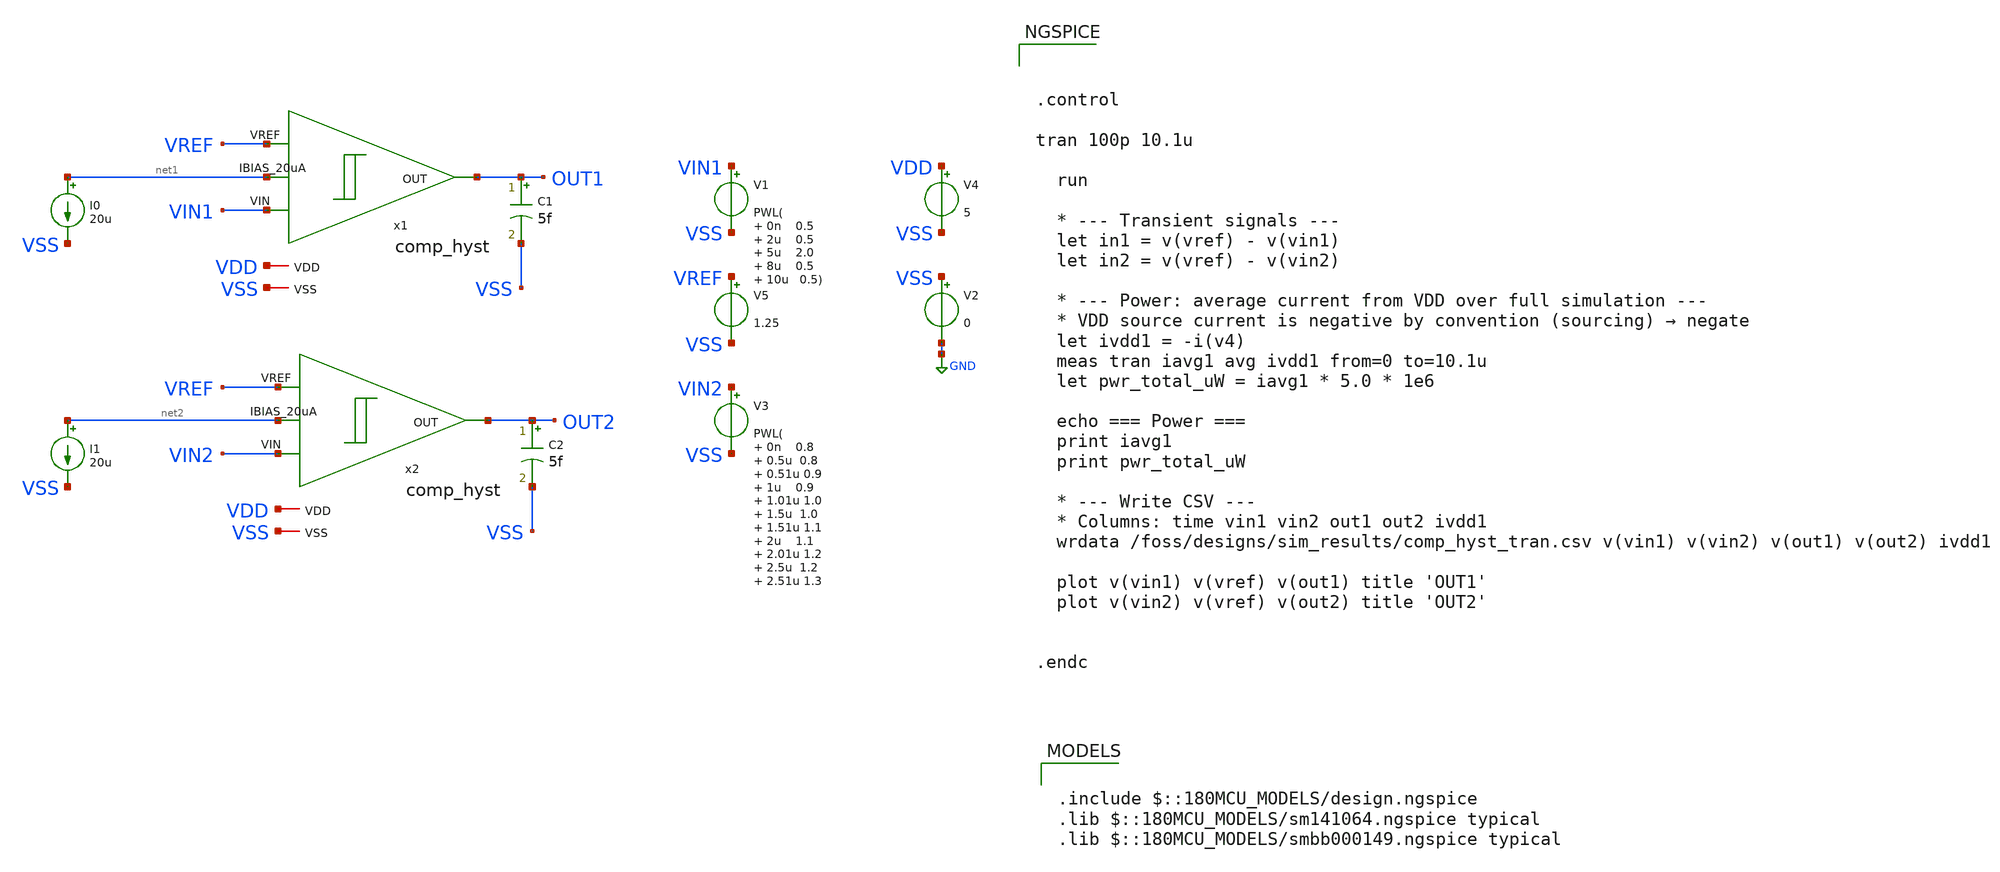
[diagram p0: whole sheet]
** sch_path: designs/hyst-comparator/tb_tran_comp_hyst.sch
**.subckt tb_tran_comp_hyst
I0 net1 VSS 20u
I1 net2 VSS 20u
C1 OUT1 VSS 5f m=1
C2 OUT2 VSS 5f m=1
V1 VIN1 VSS PWL( 0n 0.5 2u 0.5 5u 2.0 8u 0.5 10u 0.5)
V3 VIN2 VSS PWL( 0n 0.8 0.5u 0.8 0.51u 0.9 1u 0.9 1.01u 1.0 1.5u 1.0 1.51u 1.1 2u 1.1 2.01u 1.2 2.5u
+ 1.2 2.51u 1.3 3u 1.3 3.01u 1.4 3.5u 1.4 3.51u 1.5 4u 1.5 4.01u 1.6 4.5u 1.6 4.51u 1.5 5u 1.5 5.01u 1.4
+ 5.5u 1.4 5.51u 1.3 6u 1.3 6.01u 1.2 6.5u 1.2 6.51u 1.1 7u 1.1 7.01u 1.0 7.5u 1.0 7.51u 0.9 8u 0.9 8.01u
+ 0.8 10u 0.8)
V4 VDD VSS 5
V5 VREF VSS 1.25
V2 VSS GND 0
x1 VDD net1 VIN1 VREF OUT1 VSS comp_hyst
x2 VDD net2 VIN2 VREF OUT2 VSS comp_hyst
**** begin user architecture code



.control

tran 100p 10.1u

  run

  * --- Transient signals ---
  let in1 = v(vref) - v(vin1)
  let in2 = v(vref) - v(vin2)

  * --- Power: average current from VDD over full simulation ---
  * VDD source current is negative by convention (sourcing) → negate
  let ivdd1 = -i(v4)
  meas tran iavg1 avg ivdd1 from=0 to=10.1u
  let pwr_total_uW = iavg1 * 5.0 * 1e6

  echo === Power ===
  print iavg1
  print pwr_total_uW

  * --- Write CSV ---
  * Columns: time vin1 vin2 out1 out2 ivdd1
  wrdata /foss/designs/sim_results/comp_hyst_tran.csv v(vin1) v(vin2) v(out1) v(out2) ivdd1

  plot v(vin1) v(vref) v(out1) title 'OUT1'
  plot v(vin2) v(vref) v(out2) title 'OUT2'


.endc



.include $::180MCU_MODELS/design.ngspice
.lib $::180MCU_MODELS/sm141064.ngspice typical
.lib $::180MCU_MODELS/smbb000149.ngspice typical

**** end user architecture code
**.ends

* expanding   symbol:  comp_hyst.sym # of pins=6
** sym_path: designs/hyst-comparator/comp_hyst.sym
** sch_path: designs/hyst-comparator/comp_hyst.sch
.subckt comp_hyst VDD IBIAS_20uA VIN VREF OUT VSS
*.ipin VIN
*.ipin VREF
*.opin OUT
*.ipin IBIAS_20uA
*.iopin VDD
*.iopin VSS
XM1 net2 IBIAS_20uA VDD VDD pfet_05v0 L=1u W=11.8u nf=1 ad='int((nf+1)/2) * W/nf * 0.18u' as='int((nf+2)/2) * W/nf * 0.18u'
+ pd='2*int((nf+1)/2) * (W/nf + 0.18u)' ps='2*int((nf+2)/2) * (W/nf + 0.18u)' nrd='0.18u / W' nrs='0.18u / W'
+ sa=0 sb=0 sd=0 m=1
XM2 IBIAS_20uA IBIAS_20uA VDD VDD pfet_05v0 L=1u W=11.8u nf=1 ad='int((nf+1)/2) * W/nf * 0.18u' as='int((nf+2)/2) * W/nf * 0.18u'
+ pd='2*int((nf+1)/2) * (W/nf + 0.18u)' ps='2*int((nf+2)/2) * (W/nf + 0.18u)' nrd='0.18u / W' nrs='0.18u / W'
+ sa=0 sb=0 sd=0 m=1
XM3 net1 net1 VDD VDD pfet_05v0 L=1u W=11.8u nf=1 ad='int((nf+1)/2) * W/nf * 0.18u' as='int((nf+2)/2) * W/nf * 0.18u'
+ pd='2*int((nf+1)/2) * (W/nf + 0.18u)' ps='2*int((nf+2)/2) * (W/nf + 0.18u)' nrd='0.18u / W' nrs='0.18u / W'
+ sa=0 sb=0 sd=0 m=1
XM4 OUT net1 VDD VDD pfet_05v0 L=1u W=11.8u nf=1 ad='int((nf+1)/2) * W/nf * 0.18u' as='int((nf+2)/2) * W/nf * 0.18u'
+ pd='2*int((nf+1)/2) * (W/nf + 0.18u)' ps='2*int((nf+2)/2) * (W/nf + 0.18u)' nrd='0.18u / W' nrs='0.18u / W'
+ sa=0 sb=0 sd=0 m=1
XM5 net4 VIN net2 VDD pfet_05v0 L=1u W=11.21u nf=1 ad='int((nf+1)/2) * W/nf * 0.18u' as='int((nf+2)/2) * W/nf * 0.18u'
+ pd='2*int((nf+1)/2) * (W/nf + 0.18u)' ps='2*int((nf+2)/2) * (W/nf + 0.18u)' nrd='0.18u / W' nrs='0.18u / W'
+ sa=0 sb=0 sd=0 m=1
XM6 net3 VREF net2 VDD pfet_05v0 L=1u W=11.21u nf=1 ad='int((nf+1)/2) * W/nf * 0.18u' as='int((nf+2)/2) * W/nf * 0.18u'
+ pd='2*int((nf+1)/2) * (W/nf + 0.18u)' ps='2*int((nf+2)/2) * (W/nf + 0.18u)' nrd='0.18u / W' nrs='0.18u / W'
+ sa=0 sb=0 sd=0 m=1
XM7 net3 net3 VSS VSS nfet_05v0 L=1u W=6.78u nf=1 ad='int((nf+1)/2) * W/nf * 0.18u' as='int((nf+2)/2) * W/nf * 0.18u'
+ pd='2*int((nf+1)/2) * (W/nf + 0.18u)' ps='2*int((nf+2)/2) * (W/nf + 0.18u)' nrd='0.18u / W' nrs='0.18u / W'
+ sa=0 sb=0 sd=0 m=1
XM8 net4 net3 VSS VSS nfet_05v0 L=1u W=27.12u nf=1 ad='int((nf+1)/2) * W/nf * 0.18u' as='int((nf+2)/2) * W/nf * 0.18u'
+ pd='2*int((nf+1)/2) * (W/nf + 0.18u)' ps='2*int((nf+2)/2) * (W/nf + 0.18u)' nrd='0.18u / W' nrs='0.18u / W'
+ sa=0 sb=0 sd=0 m=1
XM9 net3 net4 VSS VSS nfet_05v0 L=1u W=27.12u nf=1 ad='int((nf+1)/2) * W/nf * 0.18u' as='int((nf+2)/2) * W/nf * 0.18u'
+ pd='2*int((nf+1)/2) * (W/nf + 0.18u)' ps='2*int((nf+2)/2) * (W/nf + 0.18u)' nrd='0.18u / W' nrs='0.18u / W'
+ sa=0 sb=0 sd=0 m=1
XM10 net4 net4 VSS VSS nfet_05v0 L=1u W=6.78u nf=1 ad='int((nf+1)/2) * W/nf * 0.18u' as='int((nf+2)/2) * W/nf * 0.18u'
+ pd='2*int((nf+1)/2) * (W/nf + 0.18u)' ps='2*int((nf+2)/2) * (W/nf + 0.18u)' nrd='0.18u / W' nrs='0.18u / W'
+ sa=0 sb=0 sd=0 m=1
XM11 net1 net4 VSS VSS nfet_05v0 L=1u W=6.78u nf=1 ad='int((nf+1)/2) * W/nf * 0.18u' as='int((nf+2)/2) * W/nf * 0.18u'
+ pd='2*int((nf+1)/2) * (W/nf + 0.18u)' ps='2*int((nf+2)/2) * (W/nf + 0.18u)' nrd='0.18u / W' nrs='0.18u / W'
+ sa=0 sb=0 sd=0 m=1
XM12 OUT net3 VSS VSS nfet_05v0 L=1u W=6.78u nf=1 ad='int((nf+1)/2) * W/nf * 0.18u' as='int((nf+2)/2) * W/nf * 0.18u'
+ pd='2*int((nf+1)/2) * (W/nf + 0.18u)' ps='2*int((nf+2)/2) * (W/nf + 0.18u)' nrd='0.18u / W' nrs='0.18u / W'
+ sa=0 sb=0 sd=0 m=1
.ends

.GLOBAL GND
.end
